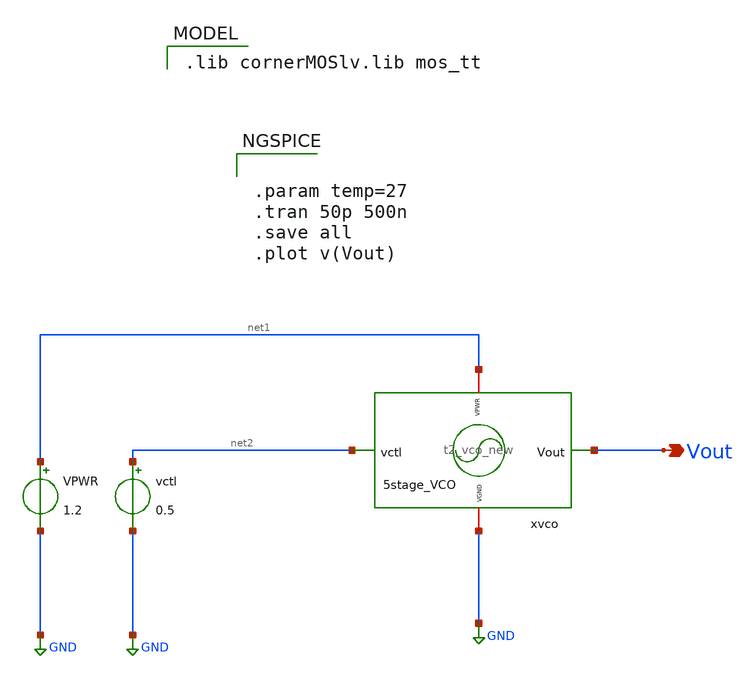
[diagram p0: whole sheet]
** sch_path: Team Designs/Team 2 Design/design_data/xschem/t2_vco_new_tb.sch
**.subckt t2_vco_new_tb Vout
*.opin Vout
x1 net1 GND net2 Vout t2_vco_new
VPWR net1 GND 1.2
vctl net2 GND 0.5
**** begin user architecture code
 .lib cornerMOSlv.lib mos_tt



.param temp=27
.tran 50p 500n
.save all
.plot v(Vout)


**** end user architecture code
**.ends
.GLOBAL GND
.end
